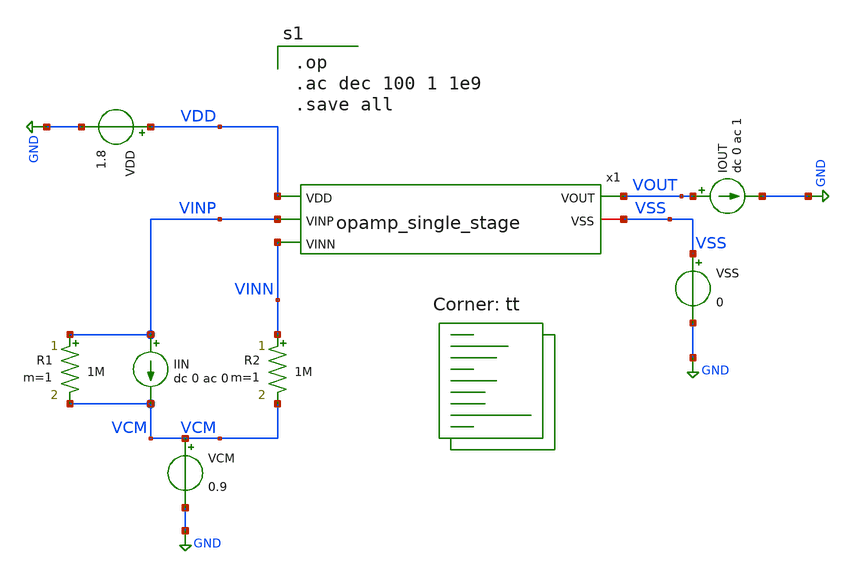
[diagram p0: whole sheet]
** sch_path: schematics/tb_impedance.sch
**.subckt tb_impedance
VDD VDD GND 1.8
R1 VINP VCM 1M m=1
R2 VINN VCM 1M m=1
VCM VCM GND 0.9
VSS VSS GND 0
IIN VINP VCM dc 0 ac 0
x1 VDD VOUT VINP VINN VSS opamp_single_stage
IOUT VOUT GND dc 0 ac 1
**** begin user architecture code

.op
.ac dec 100 1 1e9
.save all


.lib $::SKYWATER_MODELS/sky130.lib.spice tt
**** end user architecture code
**.ends
.GLOBAL GND
.end
